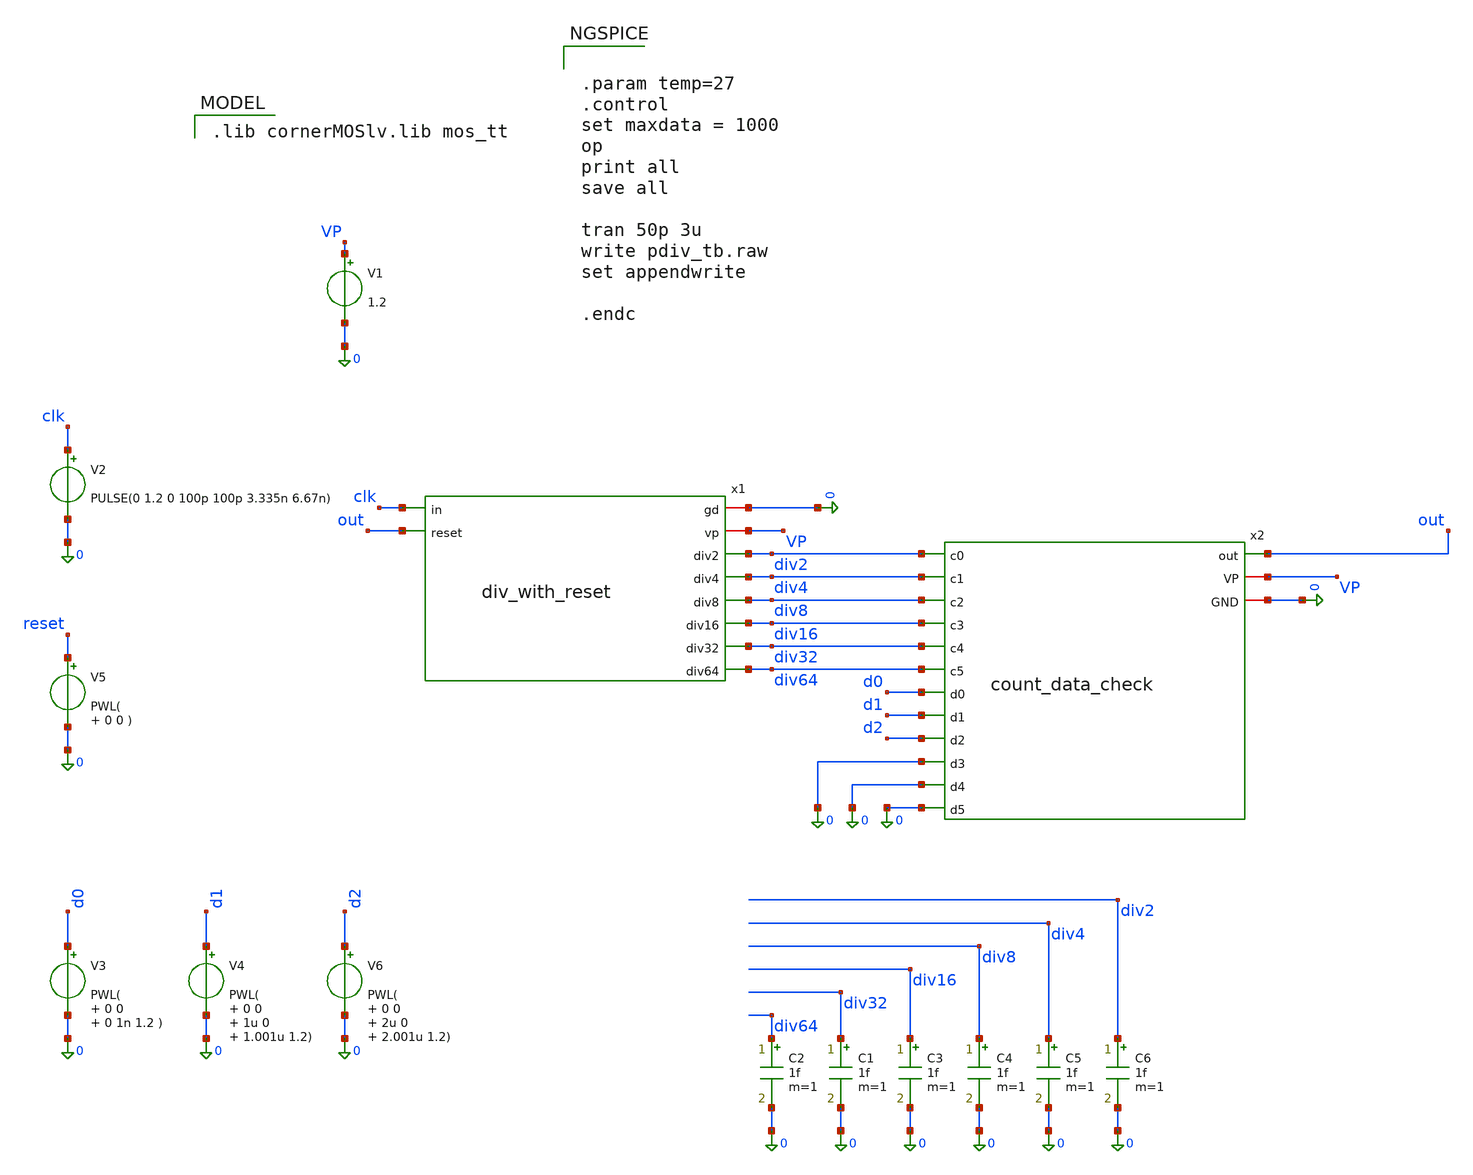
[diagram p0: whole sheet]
** sch_path: divider/tb/pdiv_sym_tb.sch
**.subckt pdiv_sym_tb
V1 VP 0 1.2
V2 clk 0 PULSE(0 1.2 0 100p 100p 3.335n 6.67n)
x1 0 VP clk out div2 div4 div8 div16 div32 div64 div_with_reset
x2 out VP 0 div2 div4 div8 div16 div32 div64 d0 d1 d2 0 0 0 count_data_check
V3 d0 0 PWL( 0 0 0 1n 1.2 )
V4 d1 0 PWL( 0 0 1u 0 1.001u 1.2)
V6 d2 0 PWL( 0 0 2u 0 2.001u 1.2)
V5 reset 0 PWL( 0 0 )
C2 div64 0 1f m=1
C1 div32 0 1f m=1
C3 div16 0 1f m=1
C4 div8 0 1f m=1
C5 div4 0 1f m=1
C6 div2 0 1f m=1
**** begin user architecture code
 .lib cornerMOSlv.lib mos_tt



.param temp=27
.control
set maxdata = 1000
op
print all
save all

tran 50p 3u
write pdiv_tb.raw
set appendwrite

.endc


**** end user architecture code
**.ends
.end
